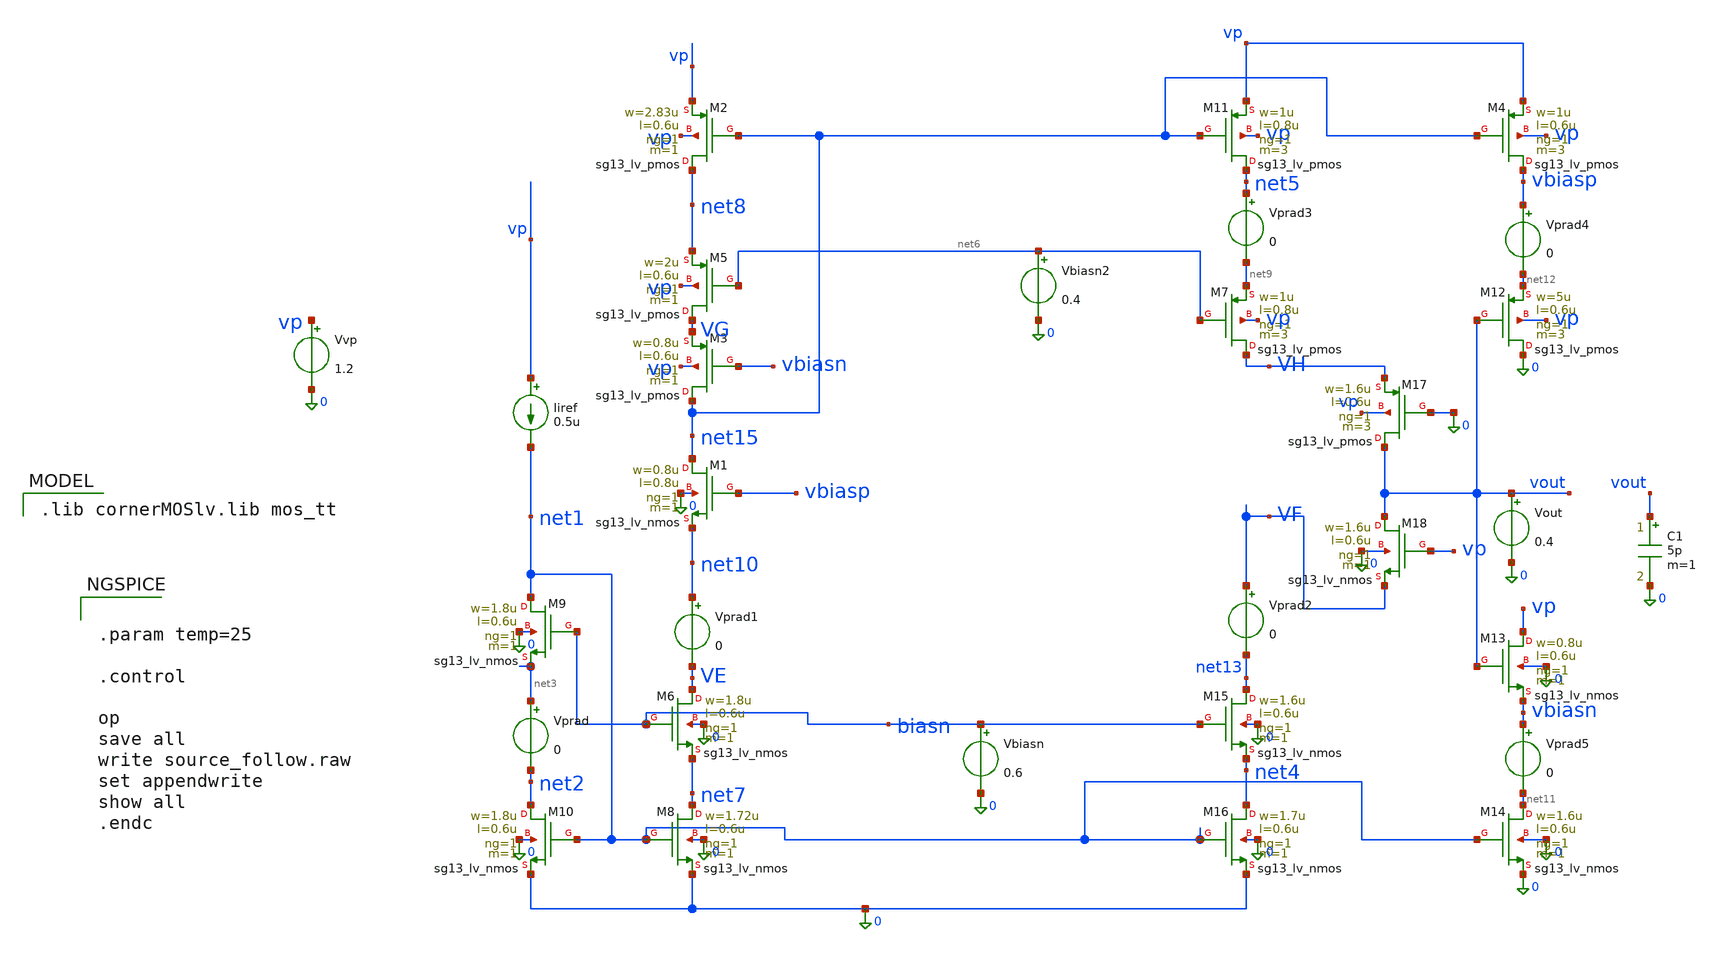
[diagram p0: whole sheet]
** sch_path: schematics/charge_pump/mirror_test_source_follower_tb.sch
**.subckt mirror_test_source_follower_tb
XM15 net13 biasn net4 0 sg13_lv_nmos w=1.6u l=0.6u ng=1 m=1 mm_ok=1
XM16 net4 net1 0 0 sg13_lv_nmos w=1.7u l=0.6u ng=1 m=1 mm_ok=1
XM1 net15 vbiasp net10 0 sg13_lv_nmos w=0.8u l=0.8u ng=1 m=1 mm_ok=1
XM6 VE biasn net7 0 sg13_lv_nmos w=1.8u l=0.6u ng=1 m=1 mm_ok=1
XM8 net7 net1 0 0 sg13_lv_nmos w=1.72u l=0.6u ng=1 m=1 mm_ok=1
XM9 net1 biasn net3 0 sg13_lv_nmos w=1.8u l=0.6u ng=1 m=1 mm_ok=1
XM10 net2 net1 0 0 sg13_lv_nmos w=1.8u l=0.6u ng=1 m=1 mm_ok=1
Vbiasn biasn 0 0.6
Vvp vp 0 1.2
Iiref vp net1 0.5u
Vprad net3 net2 0
Vprad1 net10 VE 0
Vprad2 VF net13 0
XM5 VG net6 net8 vp sg13_lv_pmos w=2u l=0.6u ng=1 m=1 mm_ok=1
XM3 net15 vbiasn VG vp sg13_lv_pmos w=0.8u l=0.6u ng=1 m=1 mm_ok=1
Vbiasn2 net6 0 0.4
XM7 VH net6 net9 vp sg13_lv_pmos w=1u l=0.8u ng=1 m=3 mm_ok=1
XM11 net5 net15 vp vp sg13_lv_pmos w=1u l=0.8u ng=1 m=3 mm_ok=1
Vprad3 net5 net9 0
XM2 net8 net15 vp vp sg13_lv_pmos w=2.83u l=0.6u ng=1 m=1 mm_ok=1
XM4 vbiasp net15 vp vp sg13_lv_pmos w=1u l=0.6u ng=1 m=3 mm_ok=1
XM12 0 vout net12 vp sg13_lv_pmos w=5u l=0.6u ng=1 m=3 mm_ok=1
XM13 vp vout vbiasn 0 sg13_lv_nmos w=0.8u l=0.6u ng=1 m=1 mm_ok=1
XM14 net11 net1 0 0 sg13_lv_nmos w=1.6u l=0.6u ng=1 m=1 mm_ok=1
XM17 vout 0 VH vp sg13_lv_pmos w=1.6u l=0.6u ng=1 m=3 mm_ok=1
XM18 vout vp VF 0 sg13_lv_nmos w=1.6u l=0.6u ng=1 m=1 mm_ok=1
C1 vout 0 5p m=1
Vout vout 0 0.4
Vprad4 vbiasp net12 0
Vprad5 vbiasn net11 0
**** begin user architecture code
 .lib cornerMOSlv.lib mos_tt



.param temp=25

.control

op
save all
write source_follow.raw
set appendwrite
show all
.endc


**** end user architecture code
**.ends
.end
